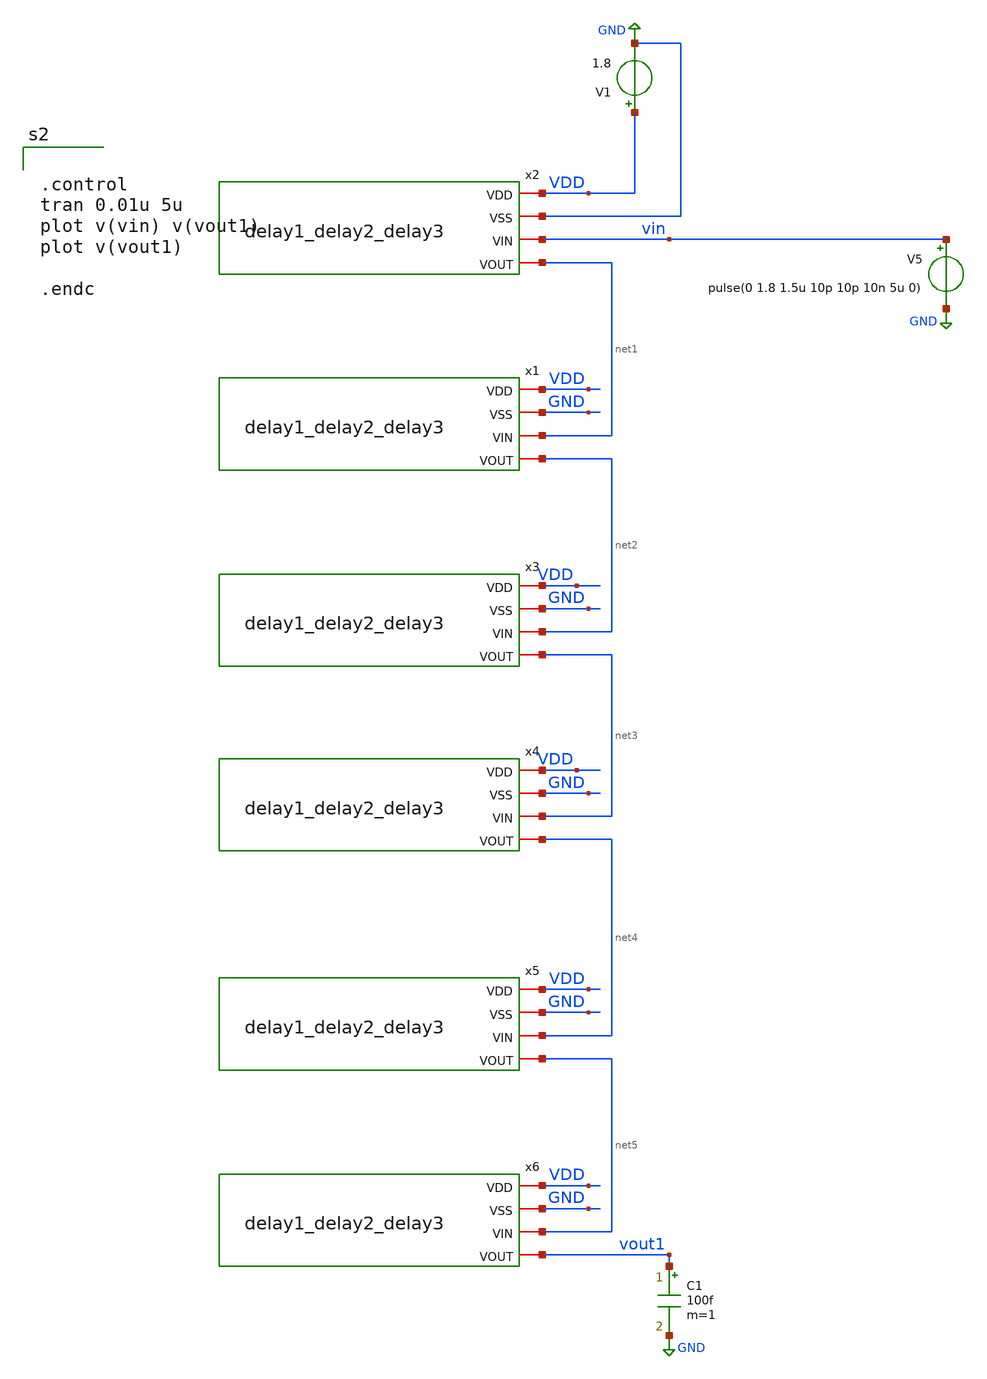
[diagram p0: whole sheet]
** sch_path: xschem/DC_DC_Converter_xschem/DC_DC_Converter/Delay_block_revised/delay123_tb.sch
**.subckt delay123_tb
x1 VDD GND net1 net2 delay1_delay2_delay3
x2 VDD GND vin net1 delay1_delay2_delay3
x3 VDD GND net2 net3 delay1_delay2_delay3
x4 VDD GND net3 net4 delay1_delay2_delay3
x5 VDD GND net4 net5 delay1_delay2_delay3
x6 VDD GND net5 vout1 delay1_delay2_delay3
V5 vin GND pulse(0 1.8 1.5u 10p 10p 10n 5u 0)
C1 vout1 GND 100f m=1
V1 VDD GND 1.8
**** begin user architecture code


.control
tran 0.01u 5u
plot v(vin) v(vout1)
plot v(vout1)

.endc



** opencircuitdesign pdks install
.lib $::SKYWATER_MODELS/sky130.lib.spice tt


**** end user architecture code
**.ends
.GLOBAL GND
.end
